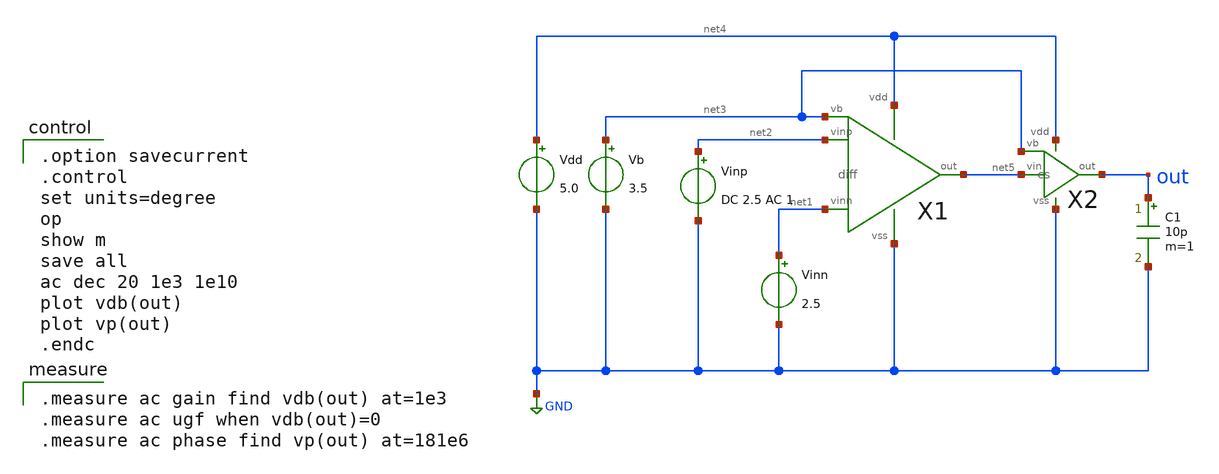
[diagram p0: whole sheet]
** sch_path: OR1/PTC06/opamp/2stage_ac.sch
**.subckt 2stage_ac
Vdd net4 GND 5.0
Vb net3 GND 3.5
Vinp net2 GND DC 2.5 AC 1
X1 net2 net1 net5 net4 GND net3 diff
X2 net5 net3 out net4 GND cs
C1 out GND 10p m=1
Vinn net1 GND 2.5
**** begin user architecture code

.option savecurrent
.control
set units=degree
op
show m
save all
ac dec 20 1e3 1e10
plot vdb(out)
plot vp(out)
.endc


.measure ac gain find vdb(out) at=1e3
.measure ac ugf when vdb(out)=0
.measure ac phase find vp(out) at=181e6

 .include $::LIB/mos.lib
.include $::LIB/passive.lib
.include $::LIB/diode.lib
**** end user architecture code
**.ends

* expanding   symbol:  diff.sym # of pins=6
** sym_path: diff.sym
** sch_path: diff.sch
.subckt diff vinp vinn out vdd vss vb
*.ipin vinn
*.ipin vinp
*.ipin vb
*.opin out
*.iopin vdd
*.iopin vss
M5 net2 vb vdd vdd pmos L=2u W=40u m=1
M1 net1 vinn net2 net2 pmos L=2u W=200u m=1
M2 out vinp net2 net2 pmos L=2u W=200u m=1
M3 net1 net1 vss vss nmos L=2u W=10u m=1
M4 out net1 vss vss nmos L=2u W=10u m=1
.ends


* expanding   symbol:  cs.sym # of pins=5
** sym_path: cs.sym
** sch_path: cs.sch
.subckt cs vin vb out vdd vss
*.ipin vb
*.ipin vin
*.opin out
*.iopin vss
*.iopin vdd
M6 out vb vdd vdd pmos L=2u W=400u m=1
M7 out vin vss vss nmos L=2u W=200u m=1
.ends

.GLOBAL GND
.end
